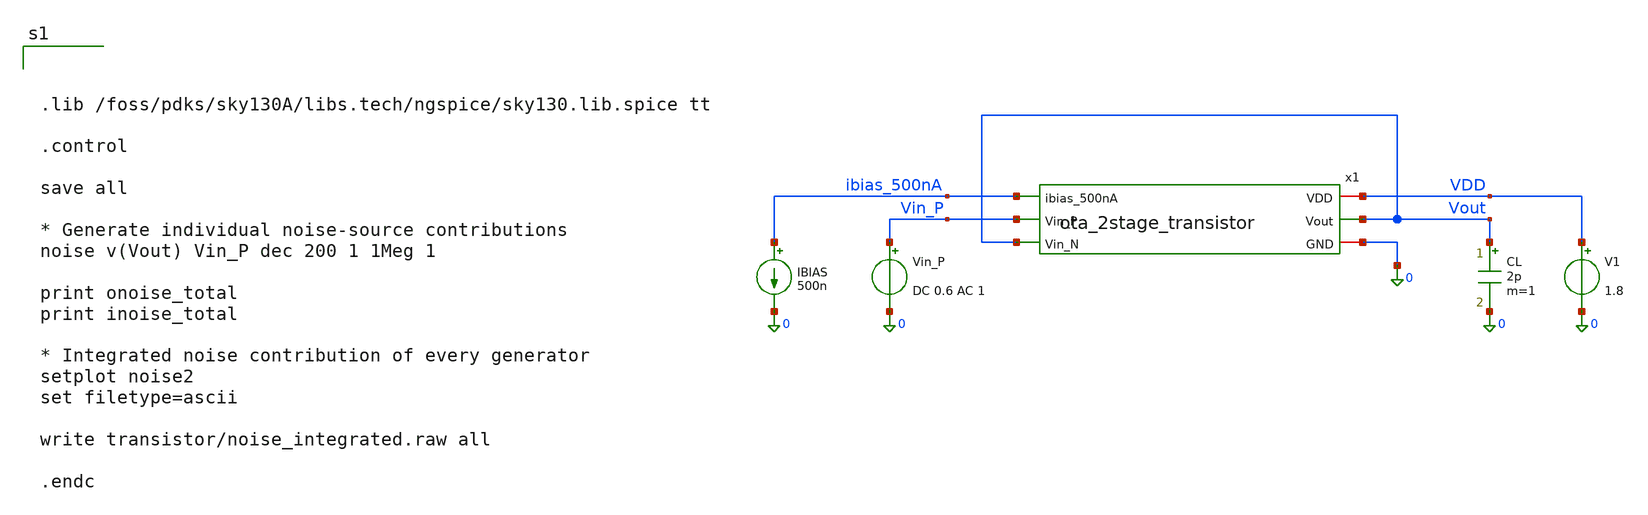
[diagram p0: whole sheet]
** sch_path: dfii/project_2stage_OTA_sim/tb_ota_2stage_noise.sch
**.subckt tb_ota_2stage_noise
x1 VDD ibias_500nA Vout Vin_P Vout 0 ota_2stage_transistor
V1 VDD 0 1.8
IBIAS ibias_500nA 0 500n
Vin_P Vin_P 0 DC 0.6 AC 1
CL Vout 0 2p m=1
**** begin user architecture code



.lib /foss/pdks/sky130A/libs.tech/ngspice/sky130.lib.spice tt

.control

save all

* Generate individual noise-source contributions
noise v(Vout) Vin_P dec 200 1 1Meg 1

print onoise_total
print inoise_total

* Integrated noise contribution of every generator
setplot noise2
set filetype=ascii

write transistor/noise_integrated.raw all

.endc



**** end user architecture code
**.ends

* expanding   symbol:
*+  /foss/designs/project_2stage_OTA/dfii/project_2stage_OTA/ota_2stage_transistor.sym # of pins=6
** sym_path: dfii/project_2stage_OTA/ota_2stage_transistor.sym
** sch_path: dfii/project_2stage_OTA/ota_2stage_transistor.sch
.subckt ota_2stage_transistor VDD ibias_500nA Vout Vin_P Vin_N GND
*.iopin VDD
*.iopin GND
*.ipin ibias_500nA
*.ipin Vin_N
*.ipin Vin_P
*.opin Vout
XNLOAD_0 vdiode_n vdiode_n GND GND sky130_fd_pr__nfet_01v8 L=12 W=3.6 nf=1 ad='int((1 + 1)/2) * 3.6 / 1 * 0.29'
+ as='int((1 + 2)/2) * 3.6 / 1 * 0.29' pd='2*int((1 + 1)/2) * (3.6 / 1 + 0.29)' ps='2*int((1 + 2)/2) * (3.6 / 1 + 0.29)'
+ nrd='0.29 / 3.6 ' nrs='0.29 / 3.6 ' sa=0 sb=0 sd=0 mult=1 m=1
XNLOAD_1 out_s1 vdiode_n GND GND sky130_fd_pr__nfet_01v8 L=12 W=3.6 nf=1 ad='int((1 + 1)/2) * 3.6 / 1 * 0.29'
+ as='int((1 + 2)/2) * 3.6 / 1 * 0.29' pd='2*int((1 + 1)/2) * (3.6 / 1 + 0.29)' ps='2*int((1 + 2)/2) * (3.6 / 1 + 0.29)'
+ nrd='0.29 / 3.6 ' nrs='0.29 / 3.6 ' sa=0 sb=0 sd=0 mult=1 m=1
XNLOAD_2 Vout out_s1 GND GND sky130_fd_pr__nfet_01v8 L=2 W=3.6 nf=1 ad='int((1 + 1)/2) * 3.6 / 1 * 0.29'
+ as='int((1 + 2)/2) * 3.6 / 1 * 0.29' pd='2*int((1 + 1)/2) * (3.6 / 1 + 0.29)' ps='2*int((1 + 2)/2) * (3.6 / 1 + 0.29)'
+ nrd='0.29 / 3.6 ' nrs='0.29 / 3.6 ' sa=0 sb=0 sd=0 mult=2 m=2
XPDIFF_N vdiode_n Vin_N VCM VCM sky130_fd_pr__pfet_01v8 L=1 W=7.4 nf=1 ad='int((1 + 1)/2) * 7.4 / 1 * 0.29'
+ as='int((1 + 2)/2) * 7.4 / 1 * 0.29' pd='2*int((1 + 1)/2) * (7.4 / 1 + 0.29)' ps='2*int((1 + 2)/2) * (7.4 / 1 + 0.29)'
+ nrd='0.29 / 7.4 ' nrs='0.29 / 7.4 ' sa=0 sb=0 sd=0 mult=12 m=12
XPDIFF_P out_s1 Vin_P VCM VCM sky130_fd_pr__pfet_01v8 L=1 W=7.4 nf=1 ad='int((1 + 1)/2) * 7.4 / 1 * 0.29'
+ as='int((1 + 2)/2) * 7.4 / 1 * 0.29' pd='2*int((1 + 1)/2) * (7.4 / 1 + 0.29)' ps='2*int((1 + 2)/2) * (7.4 / 1 + 0.29)'
+ nrd='0.29 / 7.4 ' nrs='0.29 / 7.4 ' sa=0 sb=0 sd=0 mult=12 m=12
XPTAIL_1 VCM ibias_500nA VDD VDD sky130_fd_pr__pfet_01v8 L=1 W=1.76 nf=1 ad='int((1 + 1)/2) * 1.76 / 1 * 0.29'
+ as='int((1 + 2)/2) * 1.76 / 1 * 0.29' pd='2*int((1 + 1)/2) * (1.76 / 1 + 0.29)' ps='2*int((1 + 2)/2) * (1.76 / 1 + 0.29)'
+ nrd='0.29 / 1.76 ' nrs='0.29 / 1.76 ' sa=0 sb=0 sd=0 mult=1 m=1
XPTAIL_2 Vout ibias_500nA VDD VDD sky130_fd_pr__pfet_01v8 L=1 W=1.76 nf=1 ad='int((1 + 1)/2) * 1.76 / 1 * 0.29'
+ as='int((1 + 2)/2) * 1.76 / 1 * 0.29' pd='2*int((1 + 1)/2) * (1.76 / 1 + 0.29)' ps='2*int((1 + 2)/2) * (1.76 / 1 + 0.29)'
+ nrd='0.29 / 1.76 ' nrs='0.29 / 1.76 ' sa=0 sb=0 sd=0 mult=6 m=6
XPTAIL_0 ibias_500nA ibias_500nA VDD VDD sky130_fd_pr__pfet_01v8 L=1 W=1.76 nf=1 ad='int((1 + 1)/2) * 1.76 / 1 * 0.29'
+ as='int((1 + 2)/2) * 1.76 / 1 * 0.29' pd='2*int((1 + 1)/2) * (1.76 / 1 + 0.29)' ps='2*int((1 + 2)/2) * (1.76 / 1 + 0.29)'
+ nrd='0.29 / 1.76 ' nrs='0.29 / 1.76 ' sa=0 sb=0 sd=0 mult=1 m=1
XCMILLER out_s1 net1 sky130_fd_pr__cap_mim_m3_1 W=19 L=19 MF=1 m=1
XRMILLER Vout net1 GND sky130_fd_pr__res_xhigh_po_0p35 L=31.5 mult=1 m=1
.ends

.GLOBAL VDD
.end
